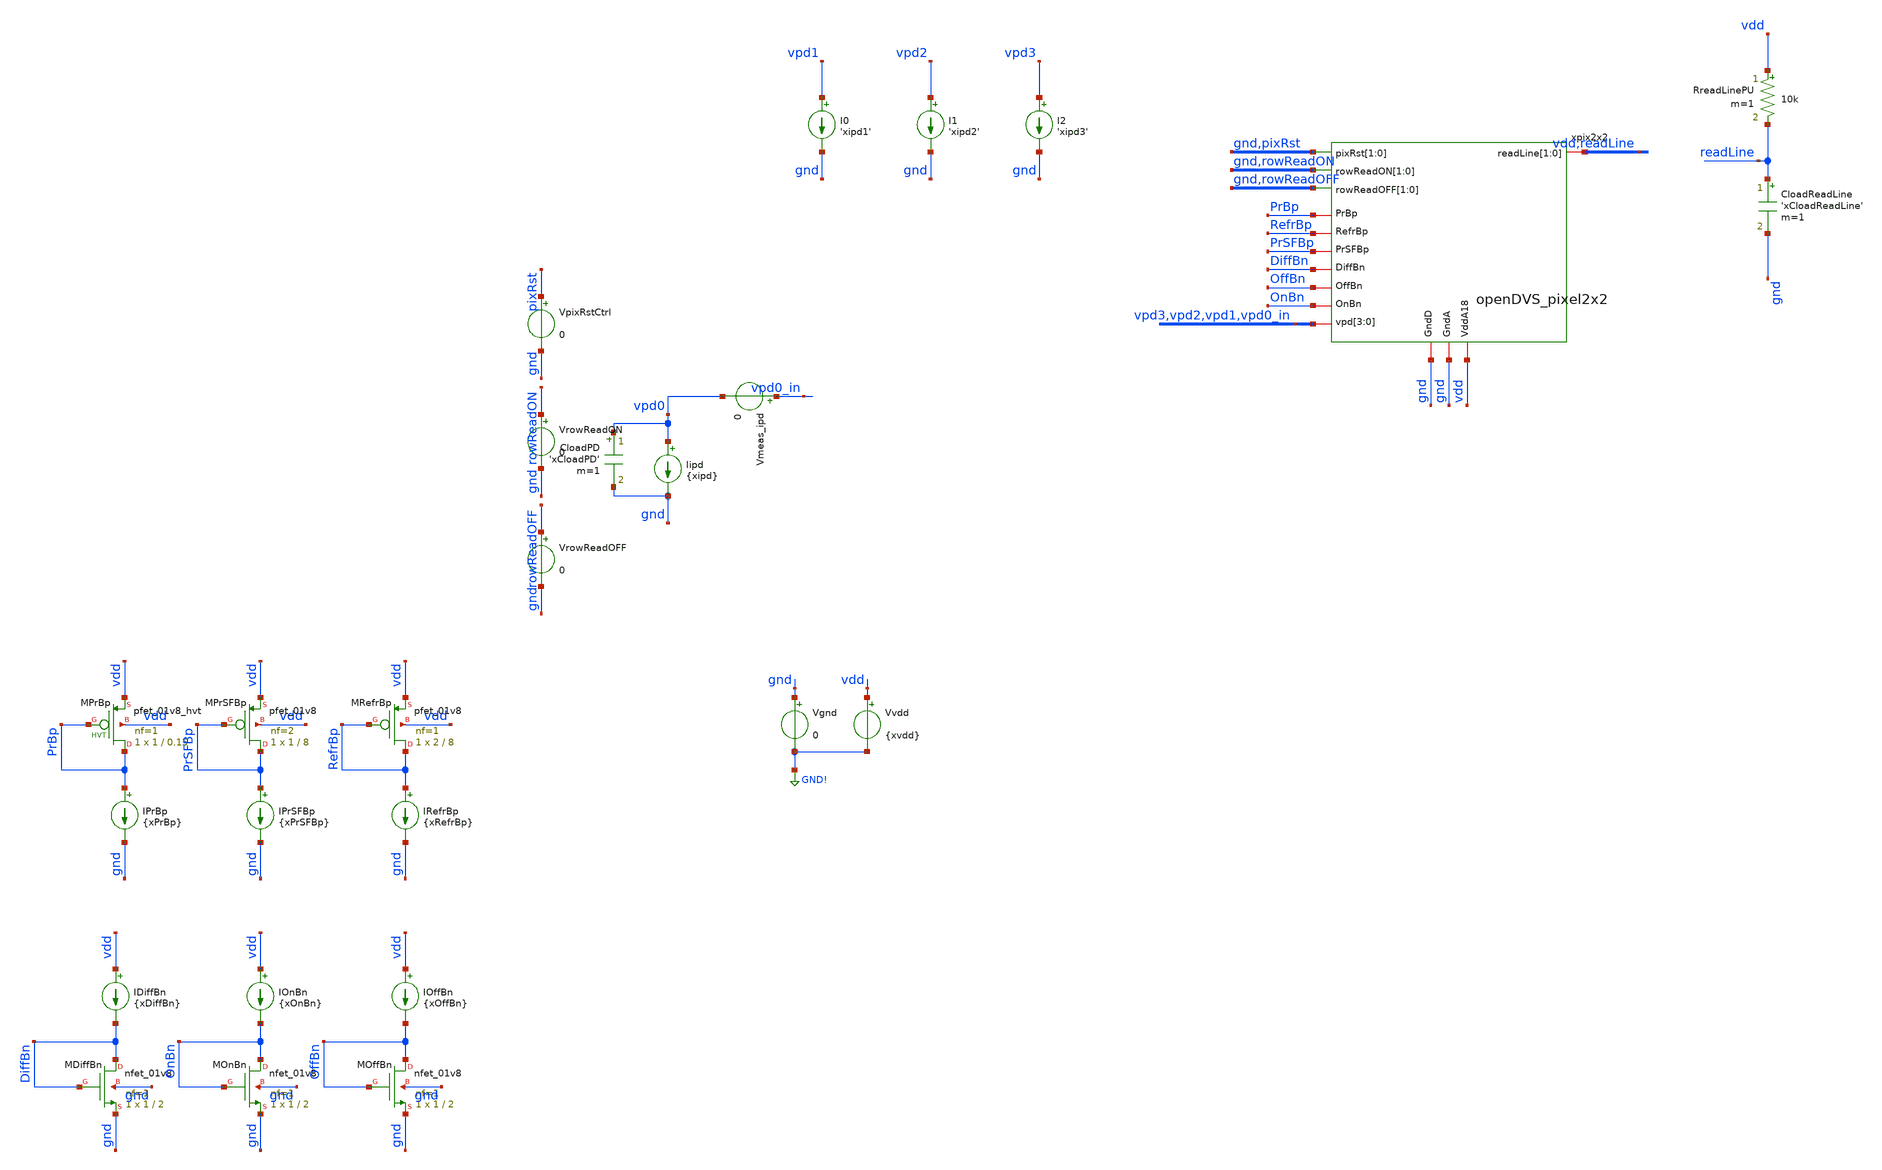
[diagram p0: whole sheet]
** sch_path: analog/klayout/production/final_merge_20260923/testbenches/cace/analog/xschem/tb_Pixel_autoreadLine_tran_2x2.sch
**.subckt tb_Pixel_autoreadLine_tran_2x2
Vgnd gnd GND! 0
Vvdd vdd GND! {xvdd}
Iipd vpd0 gnd {xipd}
IRefrBp RefrBp gnd {xRefrBp}
XMRefrBp RefrBp RefrBp vdd vdd sky130_fd_pr__pfet_01v8 L=8 W=2 nf=1 ad='int((1 + 1)/2) * 2 / 1 * 0.29'
+ as='int((1 + 2)/2) * 2 / 1 * 0.29' pd='2*int((1 + 1)/2) * (2 / 1 + 0.29)' ps='2*int((1 + 2)/2) * (2 / 1 + 0.29)'
+ nrd='0.29 / 2 ' nrs='0.29 / 2 ' sa=0 sb=0 sd=0 mult=1 m=1
IPrBp PrBp gnd {xPrBp}
XMPrBp PrBp PrBp vdd vdd sky130_fd_pr__pfet_01v8_hvt L=0.15 W=1 nf=1 ad='int((1 + 1)/2) * 1 / 1 * 0.29'
+ as='int((1 + 2)/2) * 1 / 1 * 0.29' pd='2*int((1 + 1)/2) * (1 / 1 + 0.29)' ps='2*int((1 + 2)/2) * (1 / 1 + 0.29)'
+ nrd='0.29 / 1 ' nrs='0.29 / 1 ' sa=0 sb=0 sd=0 mult=1 m=1
IPrSFBp PrSFBp gnd {xPrSFBp}
XMDiffBn DiffBn DiffBn gnd gnd sky130_fd_pr__nfet_01v8 L=2 W=1 nf=1 ad='int((1 + 1)/2) * 1 / 1 * 0.29'
+ as='int((1 + 2)/2) * 1 / 1 * 0.29' pd='2*int((1 + 1)/2) * (1 / 1 + 0.29)' ps='2*int((1 + 2)/2) * (1 / 1 + 0.29)'
+ nrd='0.29 / 1 ' nrs='0.29 / 1 ' sa=0 sb=0 sd=0 mult=1 m=1
IDiffBn vdd DiffBn {xDiffBn}
XMOnBn OnBn OnBn gnd gnd sky130_fd_pr__nfet_01v8 L=2 W=1 nf=1 ad='int((1 + 1)/2) * 1 / 1 * 0.29' as='int((1 + 2)/2) * 1 / 1 * 0.29'
+ pd='2*int((1 + 1)/2) * (1 / 1 + 0.29)' ps='2*int((1 + 2)/2) * (1 / 1 + 0.29)' nrd='0.29 / 1 ' nrs='0.29 / 1 '
+ sa=0 sb=0 sd=0 mult=1 m=1
IOnBn vdd OnBn {xOnBn}
XMOffBn OffBn OffBn gnd gnd sky130_fd_pr__nfet_01v8 L=2 W=1 nf=1 ad='int((1 + 1)/2) * 1 / 1 * 0.29' as='int((1 + 2)/2) * 1 / 1 * 0.29'
+ pd='2*int((1 + 1)/2) * (1 / 1 + 0.29)' ps='2*int((1 + 2)/2) * (1 / 1 + 0.29)' nrd='0.29 / 1 ' nrs='0.29 / 1 '
+ sa=0 sb=0 sd=0 mult=1 m=1
IOffBn vdd OffBn {xOffBn}
CloadReadLine readLine gnd 'xCloadReadLine' m=1
CloadPD vpd0 gnd 'xCloadPD' m=1
Vmeas_ipd vpd0_in vpd0 0
XMPrSFBp PrSFBp PrSFBp vdd vdd sky130_fd_pr__pfet_01v8 L=8 W=1 nf=2 ad='int((2 + 1)/2) * 1 / 2 * 0.29'
+ as='int((2 + 2)/2) * 1 / 2 * 0.29' pd='2*int((2 + 1)/2) * (1 / 2 + 0.29)' ps='2*int((2 + 2)/2) * (1 / 2 + 0.29)'
+ nrd='0.29 / 1 ' nrs='0.29 / 1 ' sa=0 sb=0 sd=0 mult=1 m=1
RreadLinePU vdd readLine 10k m=1
VpixRstCtrl pixRst gnd 0
VrowReadON rowReadON gnd 0
VrowReadOFF rowReadOFF gnd 0
xpix2x2 gnd pixRst gnd rowReadON gnd rowReadOFF vdd readLine vpd3 vpd2 vpd1 vpd0_in vdd gnd gnd OnBn
+ OffBn DiffBn PrSFBp RefrBp PrBp openDVS_pixel2x2
I0 vpd1 gnd 'xipd1'
I1 vpd2 gnd 'xipd2'
I2 vpd3 gnd 'xipd3'
**** begin user architecture code

** opencircuitdesign pdks install
.lib $::SKYWATER_MODELS/sky130.lib.spice tt



** Convergence options for nA-range weak-inversion pixel circuit
.option gmin=1e-16 abstol=1e-15 vntol=1e-9 reltol=1e-4 chgtol=1e-16
.option method=gear maxord=2 trtol=1
.option itl1=500 itl2=200 itl4=50
.option gminsteps=200 srcsteps=200
.option ramptime=100n

.param xvdd = 1.8
.param xipd = 1e-9
.param xipd1 = 1n
.param xipd2 = 1n
.param xipd3 = 1n
.param xPrBp = 10n
.param xPrSFBp = 100p
.param xRefrBp = 400p
.param xDiffBn = 5n
.param xOnBn = 200n
.param xOffBn = 0.25n

.param xCloadPD = 30f
.param xCloadReadLine = 300f

** PEX netlist includes — uncomment one
.include /home/rpgraca/research/projects/telluride/2025/nic_eventcam/nic2025_openDVS/analog/xschem/openDVS_pixel2x2_pex_simple.spice
*.include /home/rpgraca/research/projects/telluride/2025/nic_eventcam/nic2025_openDVS/analog/xschem/openDVS_pixel2x2_pex_r.spice
*.include /home/rpgraca/research/projects/telluride/2025/nic_eventcam/nic2025_openDVS/analog/xschem/openDVS_pixel2x2_pex_cc.spice
*.include /home/rpgraca/research/projects/telluride/2025/nic_eventcam/nic2025_openDVS/analog/xschem/openDVS_pixel2x2_pex_c.spice
*.include /home/rpgraca/research/projects/telluride/2025/nic_eventcam/nic2025_openDVS/analog/xschem/openDVS_pixel2x2_pex_rcc.spice
*.include /home/rpgraca/research/projects/telluride/2025/nic_eventcam/nic2025_openDVS/analog/xschem/openDVS_pixel2x2_pex_rc.spice

*Small Iphoto testing on Pix[0]
Iphoto1 vpd0 gnd pulse(50n 100n 120m 50m 50m 59.9m 300m)
Iphoto2 vpd0 gnd pulse(50n 25n 240m 50m 50m 59.9m 300m)

.save all

** Bsource probes: mirror internal nodes to top-level names (brackets OK in SPICE deck)
Bprobe_on on_mon 0 V = v(xpix2x2.pix[0].on)
Bprobe_noff noff_mon 0 V = v(xpix2x2.pix[0].noff)

.control

** ============================================================
** Event-driven auto-read testbench
** Detects xpix.ON rising or xpix.nOFF falling, then generates
** the read sequence: rowReadON, rowReadOFF, rowReadON (reset)
** ============================================================

** Read sequence timing (parameterizable)
let xevent_delay = 1e-6
let xread_on_len = 950e-9
let xgap = 50e-9
let xread_off_len = 950e-9
let xrst_phase_len = 950e-9
let xsettle = 100e-6

let sim_end = 0.39
let tran_end = sim_end + 1

** Phase 0: let circuit initialize (10ms settling)
** tran end time must exceed sim_end to avoid resume-after-finished crash
stop when time > 10e-3
tran 1u $&tran_end uic
let vdd_val = v(vdd)[length(v(vdd))-1]
let on_thresh = 0.9 * vdd_val
let noff_thresh = 0.1 * vdd_val

echo
echo '=== Auto-read TB initialized ==='
echo '    VDD =' $&vdd_val 'V'
echo '    ON thresh =' $&on_thresh 'V'
echo '    nOFF thresh =' $&noff_thresh 'V'

** Event-driven readout loop (runs until sim_end)
let event_count = 0
let t_now = time[length(time)-1]

while t_now < $&sim_end - 1e-9
  ** Arm event breakpoints
  delete all
  stop when v(on_mon) > $&on_thresh
  stop when v(noff_mon) < $&noff_thresh
  stop when time > $&sim_end
  resume

  let t_now = time[length(time)-1]
  if t_now >= $&sim_end - 1e-9
    break
  end

  let event_count = event_count + 1
  let t_event = t_now
  echo
  echo '=== Event #' $&event_count 'at t =' $&t_event 's ==='

  ** Skip read sequence if not enough time left
  let t_seq_end = t_event + xevent_delay + xread_on_len + xgap + xread_off_len + xgap +
+ xrst_phase_len + xsettle
  if t_seq_end > $&sim_end
    echo '    Skipping read sequence - too close to sim_end'
    break
  end

  ** Wait parameterized delay before read sequence
  delete all
  let t1 = t_event + xevent_delay
  stop when time > $&t1
  resume

  ** Phase 1: rowReadON (read ON phase)
  alter vrowreadon = $&vdd_val
  delete all
  let t2 = t1 + xread_on_len
  stop when time > $&t2
  resume
  alter vrowreadon = 0

  ** Gap
  delete all
  let t3 = t2 + xgap
  stop when time > $&t3
  resume

  ** Phase 2: rowReadOFF
  alter vrowreadoff = $&vdd_val
  delete all
  let t4 = t3 + xread_off_len
  stop when time > $&t4
  resume
  alter vrowreadoff = 0

  ** Gap
  delete all
  let t5 = t4 + xgap
  stop when time > $&t5
  resume

  ** Phase 3: rowReadON (reset phase) + pixRst
  alter vrowreadon = $&vdd_val
  alter vpixrstctrl = $&vdd_val
  delete all
  let t6 = t5 + xrst_phase_len
  stop when time > $&t6
  resume
  alter vrowreadon = 0
  alter vpixrstctrl = 0

  ** Post-reset settle before re-arming event detection
  delete all
  let t7 = t6 + xsettle
  stop when time > $&t7
  resume
  let t_now = time[length(time)-1]
end

** Run to sim_end to ensure complete waveform
delete all
stop when time > $&sim_end
resume

echo
echo '=== Simulation complete:' $&event_count 'events detected ==='
setplot tran1
write tb_Pixel_autoreadLine_tran_2x2.raw
.endc


**** end user architecture code
**.ends
.GLOBAL GND!
.end
